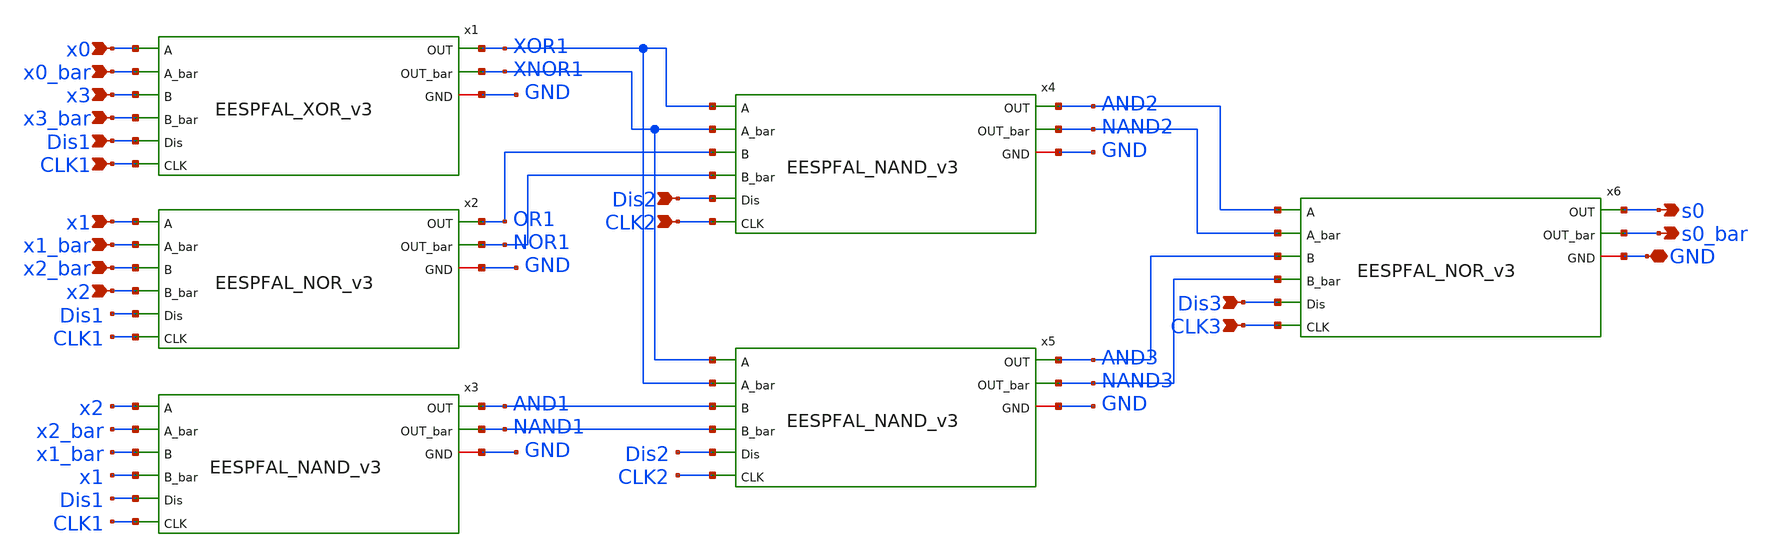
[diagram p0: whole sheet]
** sch_path: skywater_stuff/EESPFAL_s0_flat.sch
**.subckt EESPFAL_s0_flat GND x0 x0_bar x1 x1_bar x2 x2_bar x3 x3_bar CLK1 Dis1 CLK3 Dis2 CLK2 Dis3
*+ s0 s0_bar
*.iopin GND
*.ipin x0
*.ipin x0_bar
*.ipin x1
*.ipin x1_bar
*.ipin x2
*.ipin x2_bar
*.ipin x3
*.ipin x3_bar
*.ipin CLK1
*.ipin Dis1
*.ipin CLK3
*.ipin Dis2
*.ipin CLK2
*.ipin Dis3
*.opin s0
*.opin s0_bar
x1 x0 x0_bar x3 x3_bar XOR1 XNOR1 Dis1 GND CLK1 EESPFAL_XOR_v3
x4 XOR1 XNOR1 OR1 NOR1 AND2 NAND2 Dis2 GND CLK2 EESPFAL_NAND_v3
x5 XNOR1 XOR1 AND1 NAND1 AND3 NAND3 Dis2 GND CLK2 EESPFAL_NAND_v3
x6 AND2 NAND2 AND3 NAND3 s0 s0_bar Dis3 GND CLK3 EESPFAL_NOR_v3
x2 x1 x1_bar x2_bar x2 OR1 NOR1 Dis1 GND CLK1 EESPFAL_NOR_v3
x3 x2 x2_bar x1_bar x1 AND1 NAND1 Dis1 GND CLK1 EESPFAL_NAND_v3
**.ends
.end
